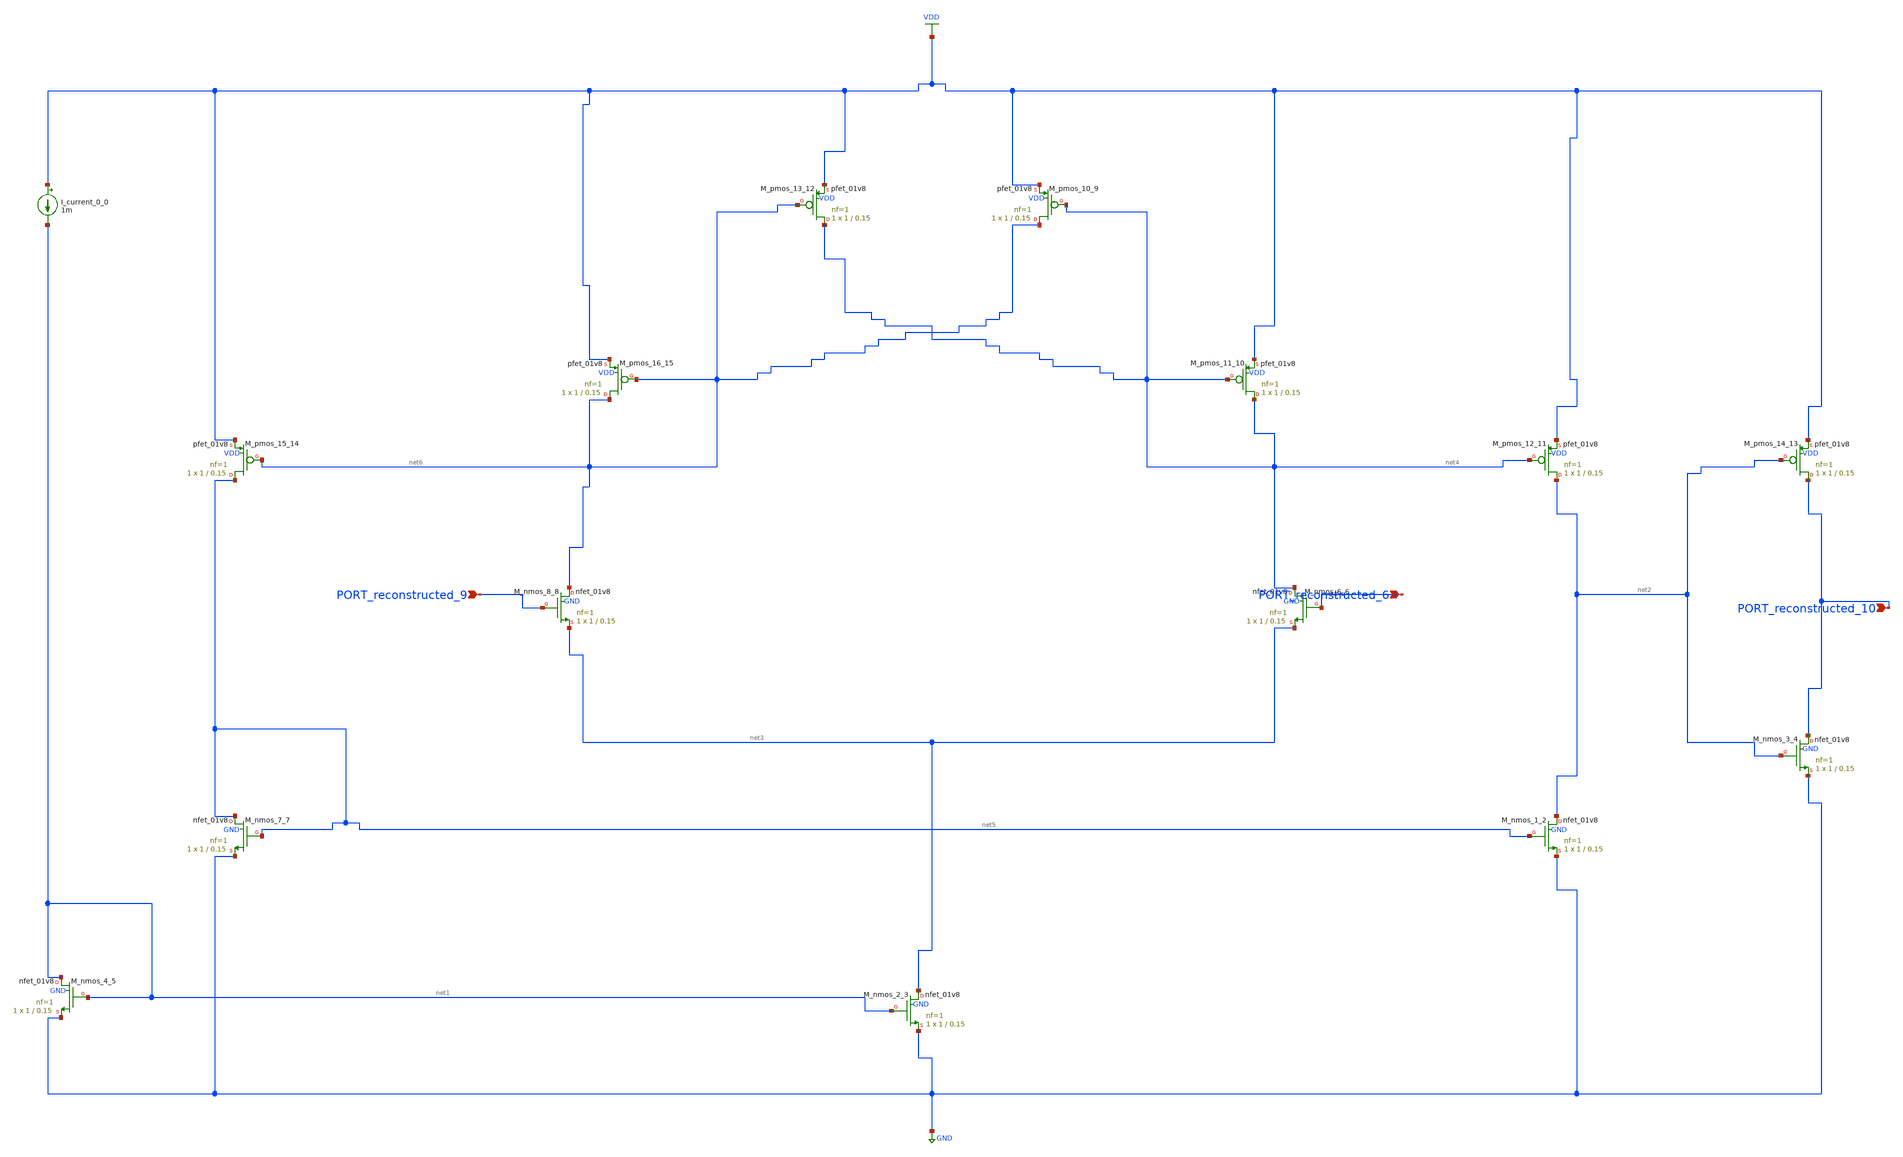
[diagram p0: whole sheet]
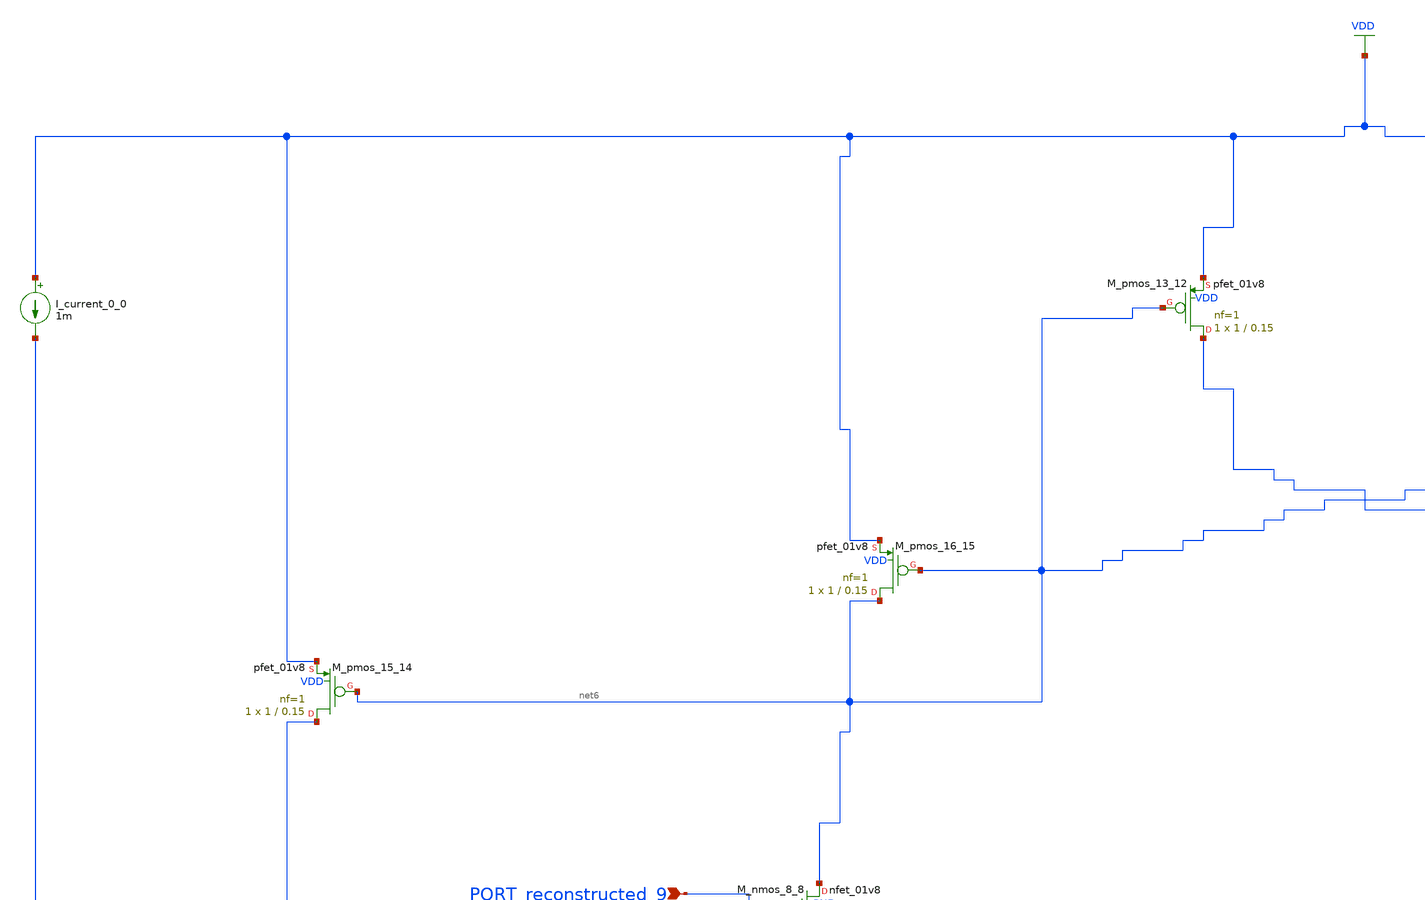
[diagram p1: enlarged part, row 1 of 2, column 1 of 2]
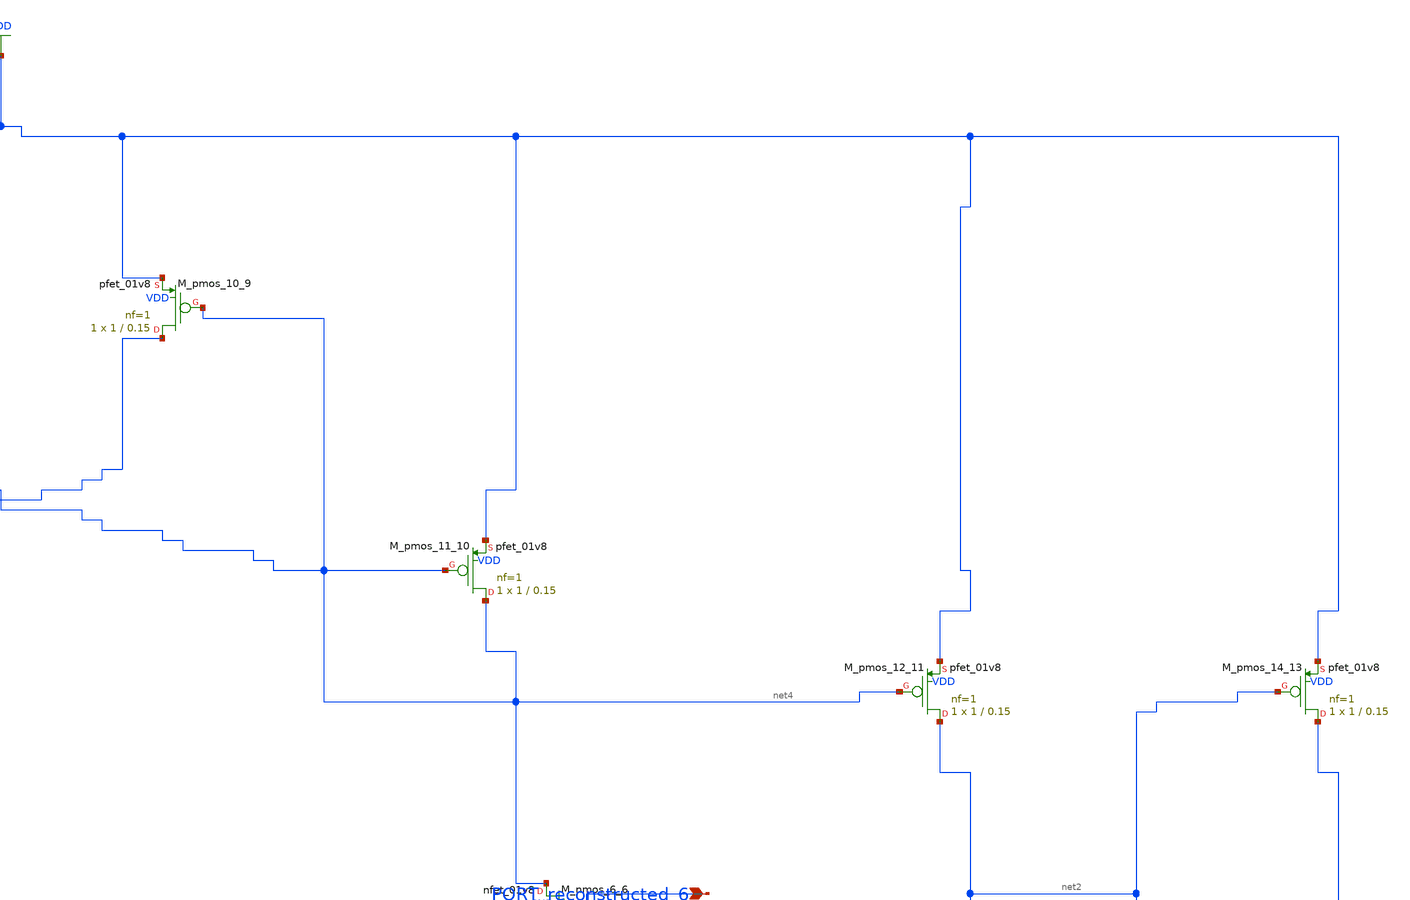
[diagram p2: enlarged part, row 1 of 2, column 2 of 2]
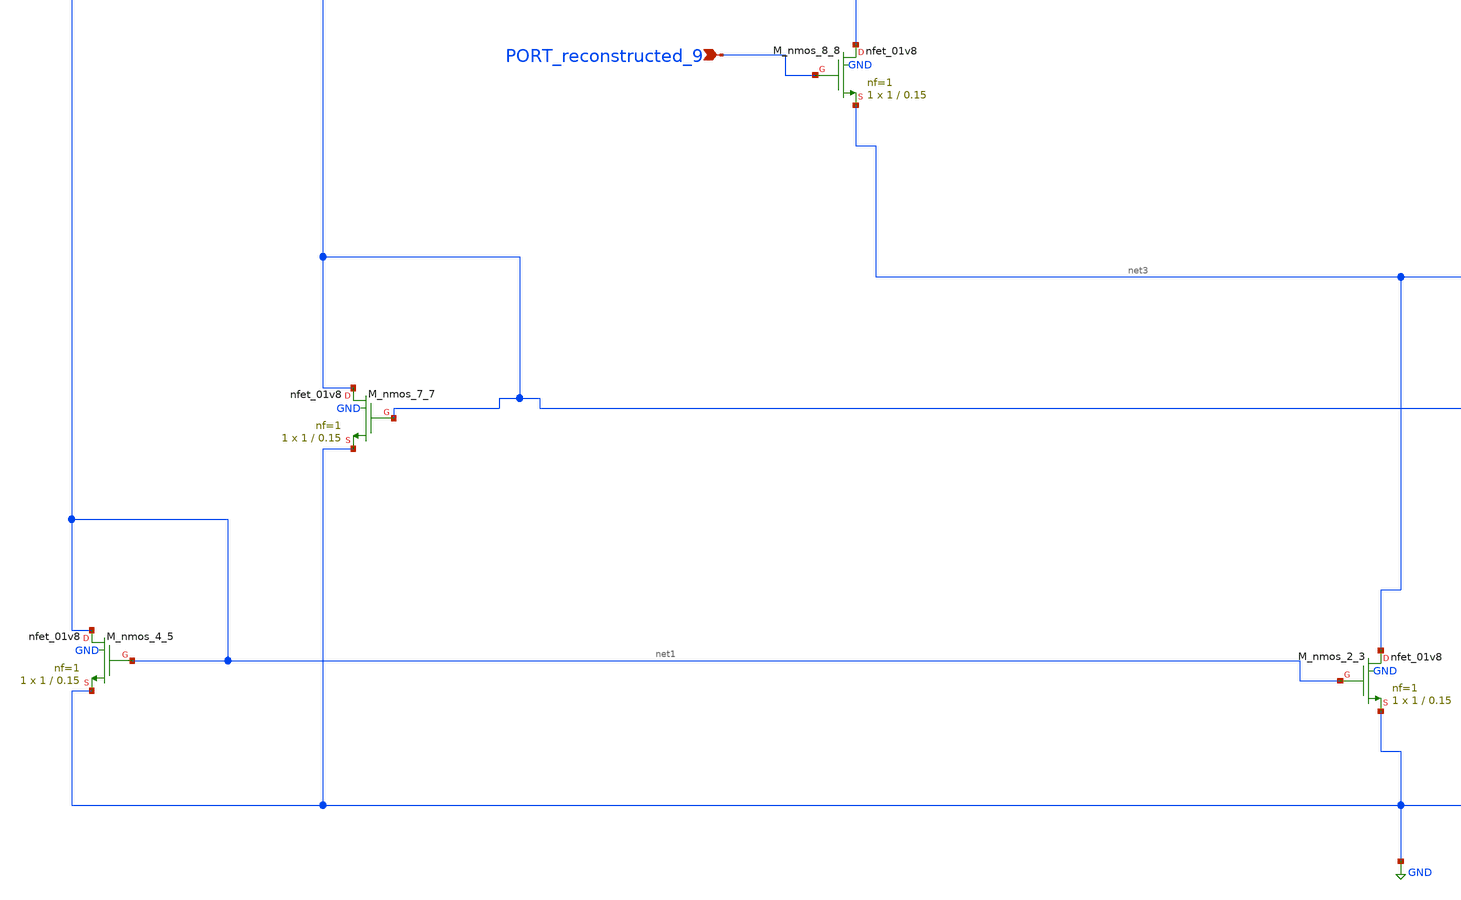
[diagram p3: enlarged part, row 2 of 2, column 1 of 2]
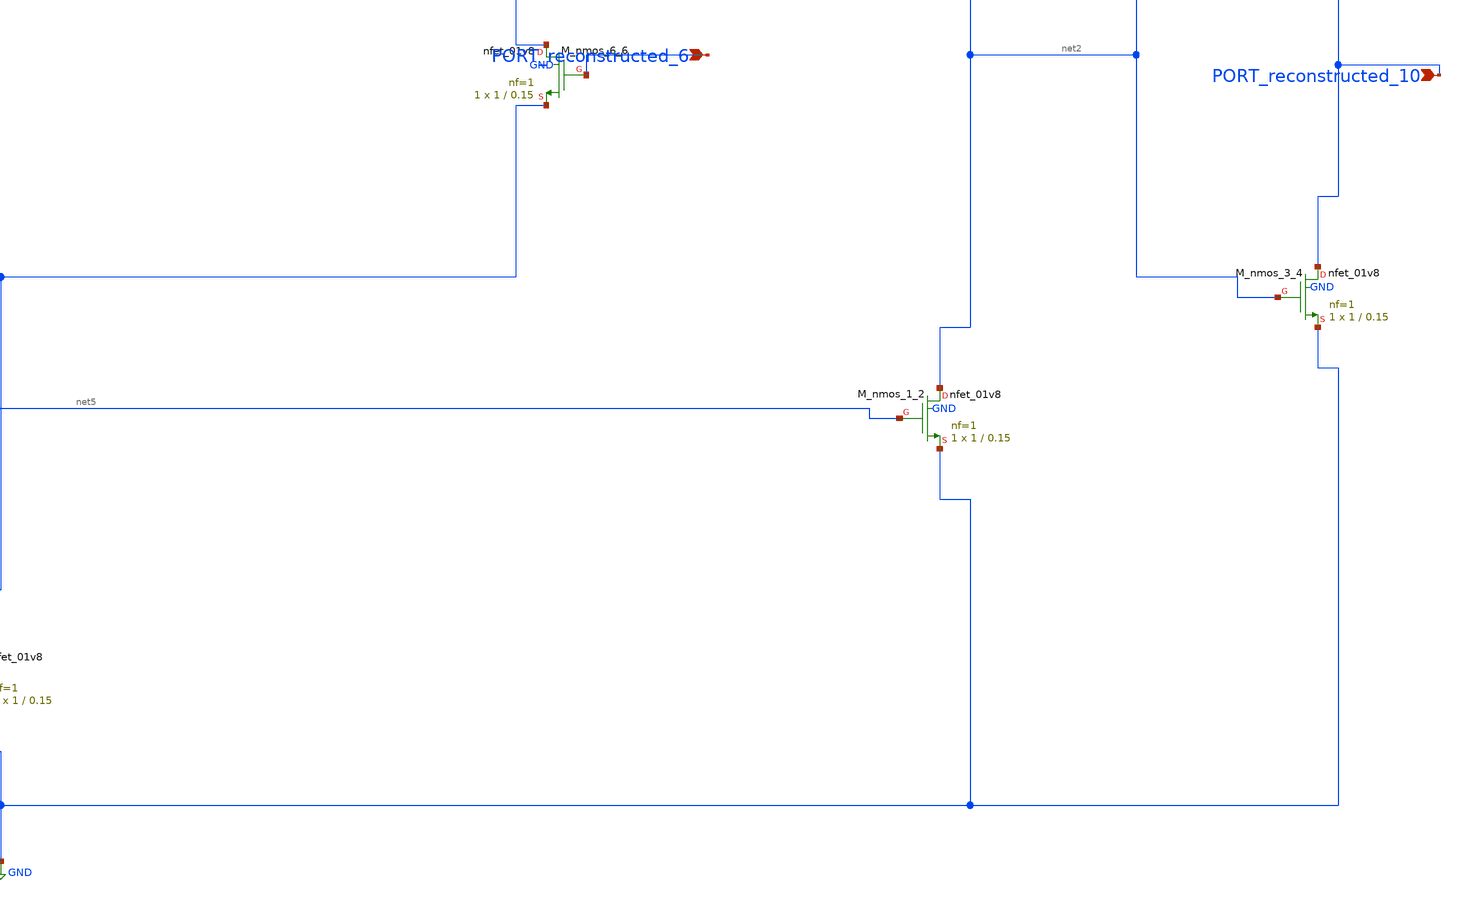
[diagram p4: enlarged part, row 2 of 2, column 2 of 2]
** sch_path: schematics/SchemGen/10_37394_232016_2021_16_27_07_003.sch
**.subckt 10_37394_232016_2021_16_27_07_003 PORT_reconstructed_6 PORT_reconstructed_10
*+ PORT_reconstructed_9
*.ipin PORT_reconstructed_6
*.ipin PORT_reconstructed_10
*.ipin PORT_reconstructed_9
I_current_0_0 VDD net1 1m
XM_nmos_1_2 net2 net5 GND GND sky130_fd_pr__nfet_01v8 L=0.15 W=1 nf=1 ad='int((1 + 1)/2) * 1 / 1 * 0.29'
+ as='int((1 + 2)/2) * 1 / 1 * 0.29' pd='2*int((1 + 1)/2) * (1 / 1 + 0.29)' ps='2*int((1 + 2)/2) * (1 / 1 + 0.29)'
+ nrd='0.29 / 1 ' nrs='0.29 / 1 ' sa=0 sb=0 sd=0 mult=1 m=1
XM_nmos_2_3 net3 net1 GND GND sky130_fd_pr__nfet_01v8 L=0.15 W=1 nf=1 ad='int((1 + 1)/2) * 1 / 1 * 0.29'
+ as='int((1 + 2)/2) * 1 / 1 * 0.29' pd='2*int((1 + 1)/2) * (1 / 1 + 0.29)' ps='2*int((1 + 2)/2) * (1 / 1 + 0.29)'
+ nrd='0.29 / 1 ' nrs='0.29 / 1 ' sa=0 sb=0 sd=0 mult=1 m=1
XM_nmos_3_4 PORT_reconstructed_10 net2 GND GND sky130_fd_pr__nfet_01v8 L=0.15 W=1 nf=1 ad='int((1 + 1)/2) * 1 / 1 * 0.29'
+ as='int((1 + 2)/2) * 1 / 1 * 0.29' pd='2*int((1 + 1)/2) * (1 / 1 + 0.29)' ps='2*int((1 + 2)/2) * (1 / 1 + 0.29)'
+ nrd='0.29 / 1 ' nrs='0.29 / 1 ' sa=0 sb=0 sd=0 mult=1 m=1
XM_nmos_4_5 net1 net1 GND GND sky130_fd_pr__nfet_01v8 L=0.15 W=1 nf=1 ad='int((1 + 1)/2) * 1 / 1 * 0.29'
+ as='int((1 + 2)/2) * 1 / 1 * 0.29' pd='2*int((1 + 1)/2) * (1 / 1 + 0.29)' ps='2*int((1 + 2)/2) * (1 / 1 + 0.29)'
+ nrd='0.29 / 1 ' nrs='0.29 / 1 ' sa=0 sb=0 sd=0 mult=1 m=1
XM_nmos_6_6 net4 PORT_reconstructed_6 net3 GND sky130_fd_pr__nfet_01v8 L=0.15 W=1 nf=1 ad='int((1 + 1)/2) * 1 / 1 * 0.29'
+ as='int((1 + 2)/2) * 1 / 1 * 0.29' pd='2*int((1 + 1)/2) * (1 / 1 + 0.29)' ps='2*int((1 + 2)/2) * (1 / 1 + 0.29)'
+ nrd='0.29 / 1 ' nrs='0.29 / 1 ' sa=0 sb=0 sd=0 mult=1 m=1
XM_nmos_7_7 net5 net5 GND GND sky130_fd_pr__nfet_01v8 L=0.15 W=1 nf=1 ad='int((1 + 1)/2) * 1 / 1 * 0.29'
+ as='int((1 + 2)/2) * 1 / 1 * 0.29' pd='2*int((1 + 1)/2) * (1 / 1 + 0.29)' ps='2*int((1 + 2)/2) * (1 / 1 + 0.29)'
+ nrd='0.29 / 1 ' nrs='0.29 / 1 ' sa=0 sb=0 sd=0 mult=1 m=1
XM_nmos_8_8 net6 PORT_reconstructed_9 net3 GND sky130_fd_pr__nfet_01v8 L=0.15 W=1 nf=1 ad='int((1 + 1)/2) * 1 / 1 * 0.29'
+ as='int((1 + 2)/2) * 1 / 1 * 0.29' pd='2*int((1 + 1)/2) * (1 / 1 + 0.29)' ps='2*int((1 + 2)/2) * (1 / 1 + 0.29)'
+ nrd='0.29 / 1 ' nrs='0.29 / 1 ' sa=0 sb=0 sd=0 mult=1 m=1
XM_pmos_10_9 net6 net4 VDD VDD sky130_fd_pr__pfet_01v8 L=0.15 W=1 nf=1 ad='int((1 + 1)/2) * 1 / 1 * 0.29'
+ as='int((1 + 2)/2) * 1 / 1 * 0.29' pd='2*int((1 + 1)/2) * (1 / 1 + 0.29)' ps='2*int((1 + 2)/2) * (1 / 1 + 0.29)'
+ nrd='0.29 / 1 ' nrs='0.29 / 1 ' sa=0 sb=0 sd=0 mult=1 m=1
XM_pmos_11_10 net4 net4 VDD VDD sky130_fd_pr__pfet_01v8 L=0.15 W=1 nf=1 ad='int((1 + 1)/2) * 1 / 1 * 0.29'
+ as='int((1 + 2)/2) * 1 / 1 * 0.29' pd='2*int((1 + 1)/2) * (1 / 1 + 0.29)' ps='2*int((1 + 2)/2) * (1 / 1 + 0.29)'
+ nrd='0.29 / 1 ' nrs='0.29 / 1 ' sa=0 sb=0 sd=0 mult=1 m=1
XM_pmos_12_11 net2 net4 VDD VDD sky130_fd_pr__pfet_01v8 L=0.15 W=1 nf=1 ad='int((1 + 1)/2) * 1 / 1 * 0.29'
+ as='int((1 + 2)/2) * 1 / 1 * 0.29' pd='2*int((1 + 1)/2) * (1 / 1 + 0.29)' ps='2*int((1 + 2)/2) * (1 / 1 + 0.29)'
+ nrd='0.29 / 1 ' nrs='0.29 / 1 ' sa=0 sb=0 sd=0 mult=1 m=1
XM_pmos_13_12 net4 net6 VDD VDD sky130_fd_pr__pfet_01v8 L=0.15 W=1 nf=1 ad='int((1 + 1)/2) * 1 / 1 * 0.29'
+ as='int((1 + 2)/2) * 1 / 1 * 0.29' pd='2*int((1 + 1)/2) * (1 / 1 + 0.29)' ps='2*int((1 + 2)/2) * (1 / 1 + 0.29)'
+ nrd='0.29 / 1 ' nrs='0.29 / 1 ' sa=0 sb=0 sd=0 mult=1 m=1
XM_pmos_14_13 PORT_reconstructed_10 net2 VDD VDD sky130_fd_pr__pfet_01v8 L=0.15 W=1 nf=1 ad='int((1 + 1)/2) * 1 / 1 * 0.29'
+ as='int((1 + 2)/2) * 1 / 1 * 0.29' pd='2*int((1 + 1)/2) * (1 / 1 + 0.29)' ps='2*int((1 + 2)/2) * (1 / 1 + 0.29)'
+ nrd='0.29 / 1 ' nrs='0.29 / 1 ' sa=0 sb=0 sd=0 mult=1 m=1
XM_pmos_15_14 net5 net6 VDD VDD sky130_fd_pr__pfet_01v8 L=0.15 W=1 nf=1 ad='int((1 + 1)/2) * 1 / 1 * 0.29'
+ as='int((1 + 2)/2) * 1 / 1 * 0.29' pd='2*int((1 + 1)/2) * (1 / 1 + 0.29)' ps='2*int((1 + 2)/2) * (1 / 1 + 0.29)'
+ nrd='0.29 / 1 ' nrs='0.29 / 1 ' sa=0 sb=0 sd=0 mult=1 m=1
XM_pmos_16_15 net6 net6 VDD VDD sky130_fd_pr__pfet_01v8 L=0.15 W=1 nf=1 ad='int((1 + 1)/2) * 1 / 1 * 0.29'
+ as='int((1 + 2)/2) * 1 / 1 * 0.29' pd='2*int((1 + 1)/2) * (1 / 1 + 0.29)' ps='2*int((1 + 2)/2) * (1 / 1 + 0.29)'
+ nrd='0.29 / 1 ' nrs='0.29 / 1 ' sa=0 sb=0 sd=0 mult=1 m=1
**.ends
.GLOBAL GND
.GLOBAL VDD
.end
